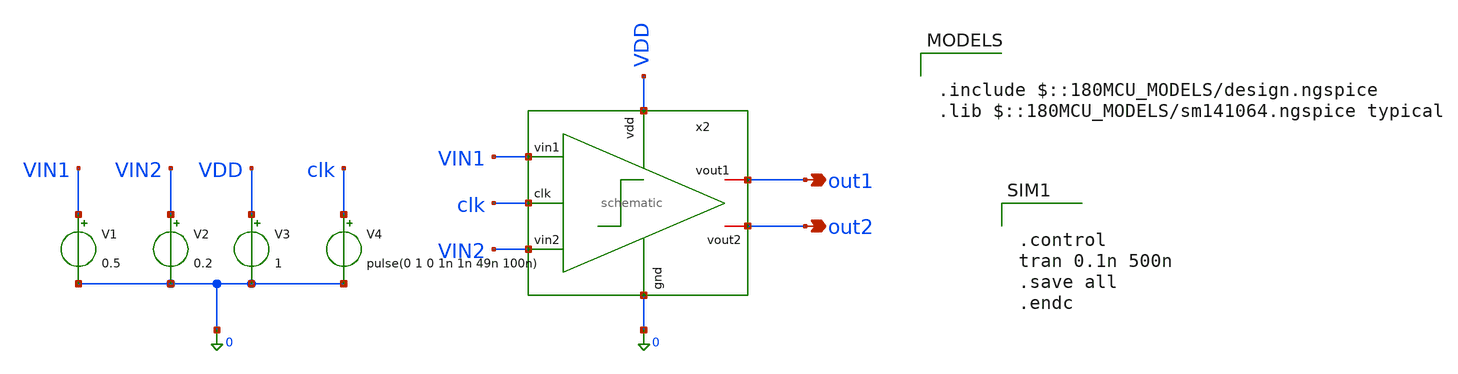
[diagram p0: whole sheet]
** sch_path: designs/DS_modulator/comparator/xschem/comparator_TB_DCIN.sch
**.subckt comparator_TB_DCIN out1 out2
*.opin out1
*.opin out2
V1 VIN1 0 0.5
V2 VIN2 0 0.2
V3 VDD 0 1
V4 clk 0 pulse(0 1 0 1n 1n 49n 100n)
x2 VDD clk out1 out2 VIN1 VIN2 0 schematic
**** begin user architecture code


.control
tran 0.1n 500n
.save all
.endc


.include $::180MCU_MODELS/design.ngspice
.lib $::180MCU_MODELS/sm141064.ngspice typical

**** end user architecture code
**.ends

* expanding   symbol:  DS_modulator/comparator/xschem/schematic.sym # of pins=7
** sym_path: designs/DS_modulator/comparator/xschem/schematic.sym
** sch_path: designs/DS_modulator/comparator/xschem/schematic.sch
.subckt schematic vdd clk vout1 vout2 vin1 vin2 gnd
*.ipin vin1
*.ipin vin2
*.ipin clk
*.ipin vdd
*.iopin vout2
*.iopin vout1
*.ipin gnd
XM1 net2 vin1 net1 net1 nfet_03v3 L=0.28u W=6u nf=1 ad='int((nf+1)/2) * W/nf * 0.18u' as='int((nf+2)/2) * W/nf * 0.18u'
+ pd='2*int((nf+1)/2) * (W/nf + 0.18u)' ps='2*int((nf+2)/2) * (W/nf + 0.18u)' nrd='0.18u / W' nrs='0.18u / W'
+ sa=0 sb=0 sd=0 m=1
XM2 vout1 vout2 vdd vdd pfet_03v3 L=0.28u W=0.5u nf=1 ad='int((nf+1)/2) * W/nf * 0.18u' as='int((nf+2)/2) * W/nf * 0.18u'
+ pd='2*int((nf+1)/2) * (W/nf + 0.18u)' ps='2*int((nf+2)/2) * (W/nf + 0.18u)' nrd='0.18u / W' nrs='0.18u / W'
+ sa=0 sb=0 sd=0 m=1
XM3 net3 vin2 net1 net1 nfet_03v3 L=0.28u W=6u nf=1 ad='int((nf+1)/2) * W/nf * 0.18u' as='int((nf+2)/2) * W/nf * 0.18u'
+ pd='2*int((nf+1)/2) * (W/nf + 0.18u)' ps='2*int((nf+2)/2) * (W/nf + 0.18u)' nrd='0.18u / W' nrs='0.18u / W'
+ sa=0 sb=0 sd=0 m=1
XM4 net1 clk gnd gnd nfet_03v3 L=0.28u W=0.5u nf=1 ad='int((nf+1)/2) * W/nf * 0.18u' as='int((nf+2)/2) * W/nf * 0.18u'
+ pd='2*int((nf+1)/2) * (W/nf + 0.18u)' ps='2*int((nf+2)/2) * (W/nf + 0.18u)' nrd='0.18u / W' nrs='0.18u / W'
+ sa=0 sb=0 sd=0 m=1
XM5 vout1 vout2 net2 net1 nfet_03v3 L=0.28u W=0.5u nf=1 ad='int((nf+1)/2) * W/nf * 0.18u' as='int((nf+2)/2) * W/nf * 0.18u'
+ pd='2*int((nf+1)/2) * (W/nf + 0.18u)' ps='2*int((nf+2)/2) * (W/nf + 0.18u)' nrd='0.18u / W' nrs='0.18u / W'
+ sa=0 sb=0 sd=0 m=1
XM6 vout2 vout1 net3 net1 nfet_03v3 L=0.28u W=0.5u nf=1 ad='int((nf+1)/2) * W/nf * 0.18u' as='int((nf+2)/2) * W/nf * 0.18u'
+ pd='2*int((nf+1)/2) * (W/nf + 0.18u)' ps='2*int((nf+2)/2) * (W/nf + 0.18u)' nrd='0.18u / W' nrs='0.18u / W'
+ sa=0 sb=0 sd=0 m=1
XM7 vout2 vout1 vdd vdd pfet_03v3 L=0.28u W=0.5u nf=1 ad='int((nf+1)/2) * W/nf * 0.18u' as='int((nf+2)/2) * W/nf * 0.18u'
+ pd='2*int((nf+1)/2) * (W/nf + 0.18u)' ps='2*int((nf+2)/2) * (W/nf + 0.18u)' nrd='0.18u / W' nrs='0.18u / W'
+ sa=0 sb=0 sd=0 m=1
XM8 vout2 clk vdd vdd pfet_03v3 L=0.28u W=2u nf=1 ad='int((nf+1)/2) * W/nf * 0.18u' as='int((nf+2)/2) * W/nf * 0.18u'
+ pd='2*int((nf+1)/2) * (W/nf + 0.18u)' ps='2*int((nf+2)/2) * (W/nf + 0.18u)' nrd='0.18u / W' nrs='0.18u / W'
+ sa=0 sb=0 sd=0 m=1
XM9 net3 clk vdd vdd pfet_03v3 L=0.28u W=2u nf=1 ad='int((nf+1)/2) * W/nf * 0.18u' as='int((nf+2)/2) * W/nf * 0.18u'
+ pd='2*int((nf+1)/2) * (W/nf + 0.18u)' ps='2*int((nf+2)/2) * (W/nf + 0.18u)' nrd='0.18u / W' nrs='0.18u / W'
+ sa=0 sb=0 sd=0 m=1
XM10 vout1 clk vdd vdd pfet_03v3 L=0.28u W=2u nf=1 ad='int((nf+1)/2) * W/nf * 0.18u' as='int((nf+2)/2) * W/nf * 0.18u'
+ pd='2*int((nf+1)/2) * (W/nf + 0.18u)' ps='2*int((nf+2)/2) * (W/nf + 0.18u)' nrd='0.18u / W' nrs='0.18u / W'
+ sa=0 sb=0 sd=0 m=1
XM11 net2 clk vdd vdd pfet_03v3 L=0.28u W=2u nf=1 ad='int((nf+1)/2) * W/nf * 0.18u' as='int((nf+2)/2) * W/nf * 0.18u'
+ pd='2*int((nf+1)/2) * (W/nf + 0.18u)' ps='2*int((nf+2)/2) * (W/nf + 0.18u)' nrd='0.18u / W' nrs='0.18u / W'
+ sa=0 sb=0 sd=0 m=1
.ends

.end
